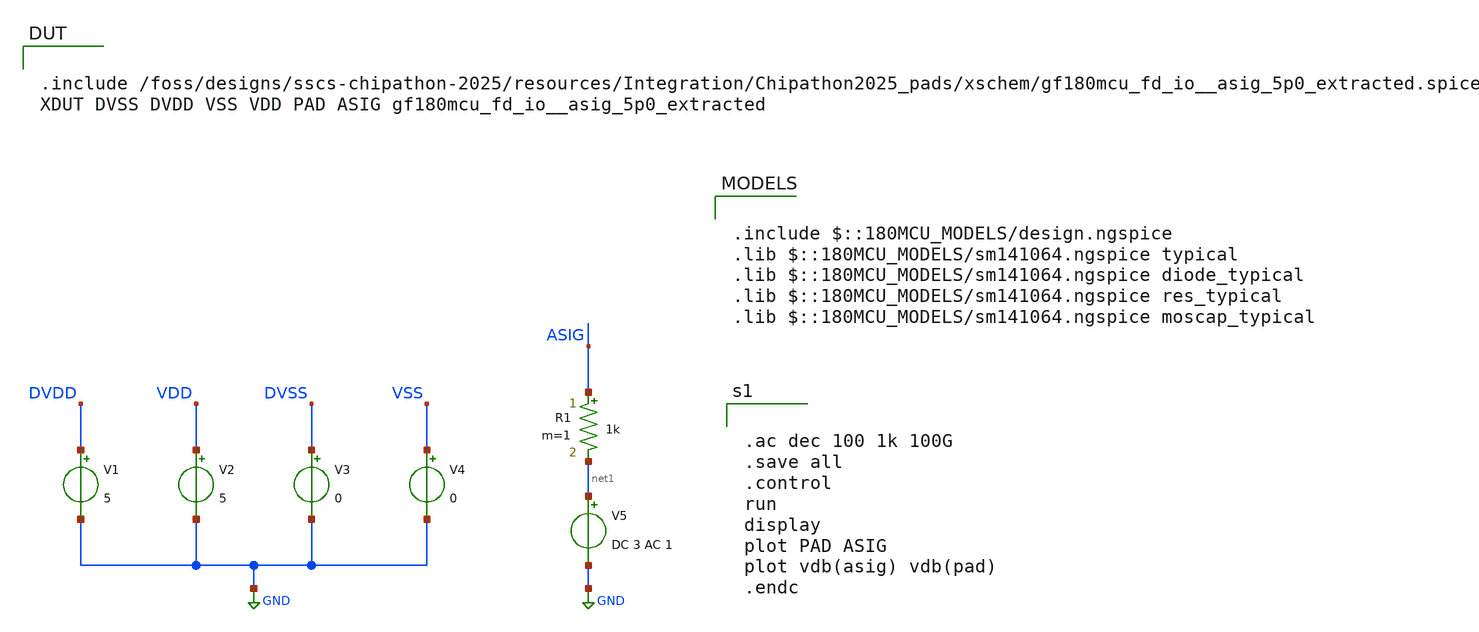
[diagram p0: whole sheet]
** sch_path: examples/pads_simulation/asig5V_AC_tb.sch
**.subckt asig5V_AC_tb
V1 DVDD GND 5
V2 VDD GND 5
V3 DVSS GND 0
V4 VSS GND 0
V5 net1 GND DC 3 AC 1
R1 ASIG net1 1k m=1
**** begin user architecture code

.include /foss/designs/sscs-chipathon-2025/resources/Integration/Chipathon2025_pads/xschem/gf180mcu_fd_io__asig_5p0_extracted.spice
XDUT DVSS DVDD VSS VDD PAD ASIG gf180mcu_fd_io__asig_5p0_extracted


.include $::180MCU_MODELS/design.ngspice
.lib $::180MCU_MODELS/sm141064.ngspice typical
.lib $::180MCU_MODELS/sm141064.ngspice diode_typical
.lib $::180MCU_MODELS/sm141064.ngspice res_typical
.lib $::180MCU_MODELS/sm141064.ngspice moscap_typical



.ac dec 100 1k 100G
.save all
.control
run
display
plot PAD ASIG
plot vdb(asig) vdb(pad)
.endc


**** end user architecture code
**.ends
.GLOBAL GND
.end
